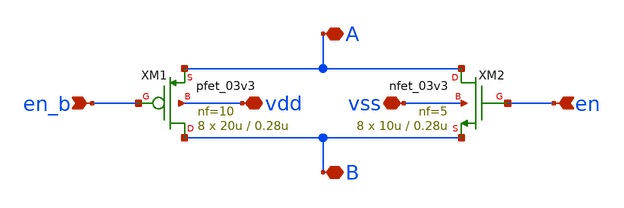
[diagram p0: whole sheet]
** sch_path: design/analog/transmission_gate/Transmission_Gate.sch
**.subckt Transmission_Gate en_b A B en vdd vss
*.ipin en_b
*.iopin A
*.iopin B
*.ipin en
*.iopin vdd
*.iopin vss
XM1 B en_b A vdd pfet_03v3 L=0.28u W=20u nf=10 ad='int((nf+1)/2) * W/nf * 0.18u' as='int((nf+2)/2) * W/nf * 0.18u'
+ pd='2*int((nf+1)/2) * (W/nf + 0.18u)' ps='2*int((nf+2)/2) * (W/nf + 0.18u)' nrd='0.18u / W' nrs='0.18u / W'
+ sa=0 sb=0 sd=0 m=8
XM2 A en B vss nfet_03v3 L=0.28u W=10u nf=5 ad='int((nf+1)/2) * W/nf * 0.18u' as='int((nf+2)/2) * W/nf * 0.18u'
+ pd='2*int((nf+1)/2) * (W/nf + 0.18u)' ps='2*int((nf+2)/2) * (W/nf + 0.18u)' nrd='0.18u / W' nrs='0.18u / W'
+ sa=0 sb=0 sd=0 m=8
**.ends
.end
